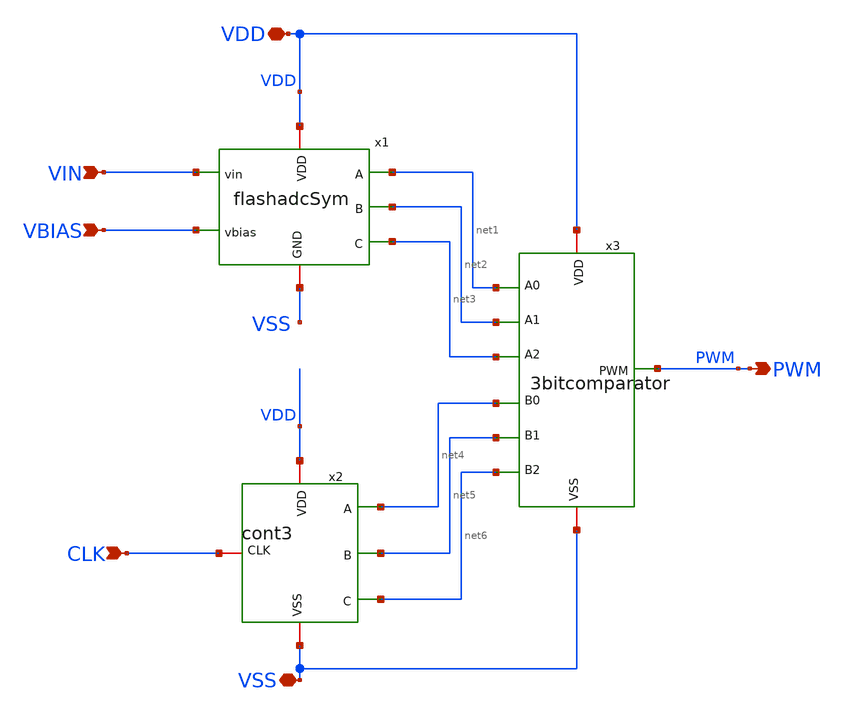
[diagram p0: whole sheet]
** sch_path: schematic/PWMADCSYM.sch
**.subckt PWMADCSYM PWM VSS VDD VIN VBIAS CLK
*.opin PWM
*.iopin VSS
*.iopin VDD
*.ipin VIN
*.ipin VBIAS
*.ipin CLK
x1 VDD VBIAS VIN VSS net1 net2 net3 flashadcSym
x2 VDD net5 net4 net6 CLK VSS cont3
x3 net6 PWM net3 net5 net2 net4 net1 VDD VSS 3bitcomparator
**.ends
.end
